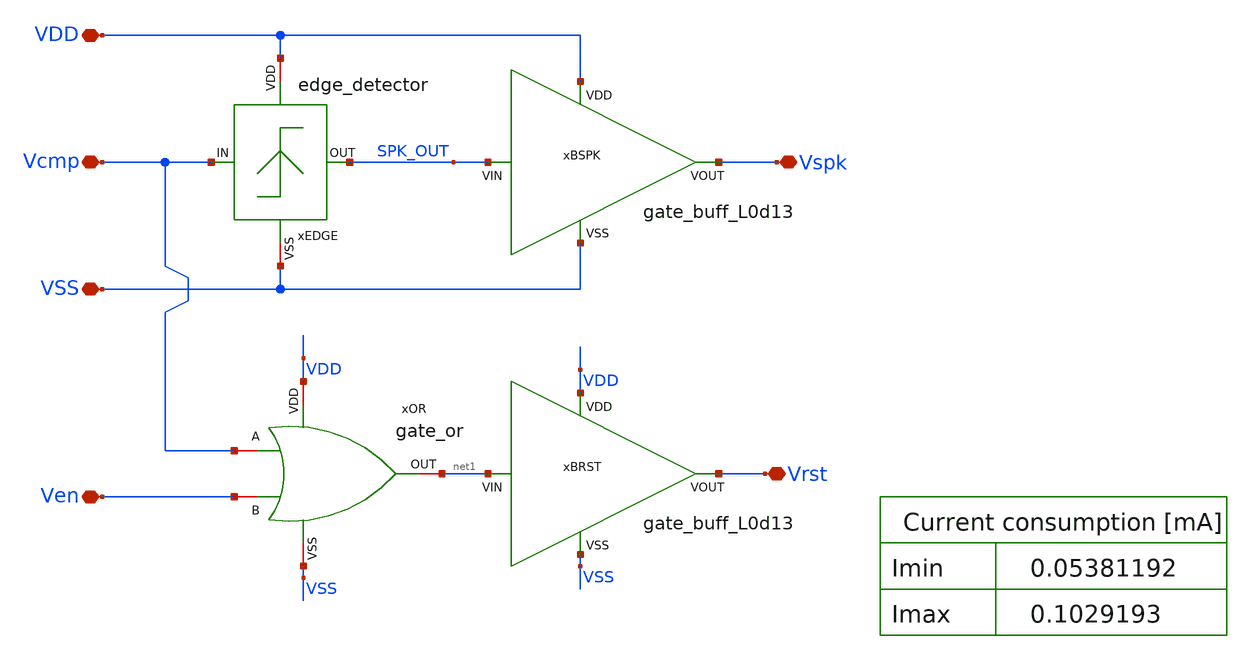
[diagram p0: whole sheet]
** sch_path: OSC9996-main/schematic/xschem/spike_generator.sch
**.subckt spike_generator Vcmp Ven Vrst Vspk VDD VSS
*.iopin Vcmp
*.iopin Ven
*.iopin Vrst
*.iopin Vspk
*.iopin VDD
*.iopin VSS
xEDGE Vcmp SPK_OUT VDD VSS edge_detector
xBSPK VDD SPK_OUT Vspk VSS gate_buff_L0d13
xBRST VDD net1 Vrst VSS gate_buff_L0d13
xOR Ven VDD VSS net1 Vcmp gate_or
**.ends
.end
